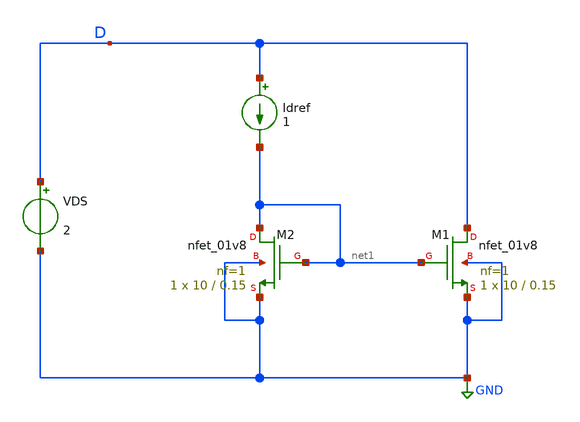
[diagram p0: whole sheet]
** sch_path: tb_ft_test.sch
**.subckt tb_ft_test
XM1 D net1 GND GND sky130_fd_pr__nfet_01v8 L=0.15 W=10 nf=1 ad='int((nf+1)/2) * W/nf * 0.29' as='int((nf+2)/2) * W/nf * 0.29'
+ pd='2*int((nf+1)/2) * (W/nf + 0.29)' ps='2*int((nf+2)/2) * (W/nf + 0.29)' nrd='0.29 / W' nrs='0.29 / W'
+ sa=0 sb=0 sd=0 mult=1 m=1
VDS D GND 2
Idref D net1 1
XM2 net1 net1 GND GND sky130_fd_pr__nfet_01v8 L=0.15 W=10 nf=1 ad='int((nf+1)/2) * W/nf * 0.29' as='int((nf+2)/2) * W/nf * 0.29'
+ pd='2*int((nf+1)/2) * (W/nf + 0.29)' ps='2*int((nf+2)/2) * (W/nf + 0.29)' nrd='0.29 / W' nrs='0.29 / W'
+ sa=0 sb=0 sd=0 mult=1 m=1
**** begin user architecture code



** Check the two ac lines below for being equal!
.options filetype=ascii
.save all

.op
.control
*dc Idref 0.1e-3 10e-3 0.1e-3

let n_idx = 101

let start_iref = 1e-6
let stop_iref = 10e-3
let delta_iref = (stop_iref - start_iref) / n_idx
let iref_act = start_iref

let gms = unitvec(n_idx)
let ids = unitvec(n_idx)

let cgss = unitvec(n_idx)
let cgds = unitvec(n_idx)

let idxs = 0
let idx = idxs

*loop
while iref_act le stop_iref
  alter idref iref_act
  run
  *print @m.xm2.msky130_fd_pr__nfet_01v8[gm]

  let gms[idx] = @m.xm2.msky130_fd_pr__nfet_01v8[gm]
  let ids[idx] = @m.xm2.msky130_fd_pr__nfet_01v8[id]

  let cgss[idx] = @m.xm2.msky130_fd_pr__nfet_01v8[cgs]
  let cgds[idx] = @m.xm2.msky130_fd_pr__nfet_01v8[cgd]

  let iref_act = iref_act + delta_iref
  let idxs = idx + 1
  let idx = idxs
end

let ft = gms/(2*3.1415*(cgss+cgds))

plot gms vs ids
plot xlog ft vs ids

.endc
.end



.include $::SKYWATER_MODELS/cells/nfet_01v8/sky130_fd_pr__nfet_01v8__tt.corner.spice
.include $::SKYWATER_MODELS/cells/nfet_01v8_lvt/sky130_fd_pr__nfet_01v8_lvt__tt.corner.spice
.include $::SKYWATER_MODELS/cells/pfet_01v8/sky130_fd_pr__pfet_01v8__tt.corner.spice
.include $::SKYWATER_MODELS/cells/nfet_03v3_nvt/sky130_fd_pr__nfet_03v3_nvt__tt.corner.spice
.include $::SKYWATER_MODELS/cells/nfet_05v0_nvt/sky130_fd_pr__nfet_05v0_nvt__tt.corner.spice
.include $::SKYWATER_MODELS/cells/esd_nfet_01v8/sky130_fd_pr__esd_nfet_01v8__tt.corner.spice
.include $::SKYWATER_MODELS/cells/pfet_01v8_lvt/sky130_fd_pr__pfet_01v8_lvt__tt.corner.spice
.include $::SKYWATER_MODELS/cells/pfet_01v8_hvt/sky130_fd_pr__pfet_01v8_hvt__tt.corner.spice
.include $::SKYWATER_MODELS/cells/esd_pfet_g5v0d10v5/sky130_fd_pr__esd_pfet_g5v0d10v5__tt.corner.spice
.include $::SKYWATER_MODELS/cells/pfet_g5v0d10v5/sky130_fd_pr__pfet_g5v0d10v5__tt.corner.spice
.include $::SKYWATER_MODELS/cells/pfet_g5v0d16v0/sky130_fd_pr__pfet_g5v0d16v0__tt.corner.spice
.include $::SKYWATER_MODELS/cells/nfet_g5v0d10v5/sky130_fd_pr__nfet_g5v0d10v5__tt.corner.spice
.include $::SKYWATER_MODELS/cells/nfet_g5v0d16v0/sky130_fd_pr__nfet_g5v0d16v0__tt_discrete.corner.spice
.include $::SKYWATER_MODELS/cells/esd_nfet_g5v0d10v5/sky130_fd_pr__esd_nfet_g5v0d10v5__tt.corner.spice
.include $::SKYWATER_MODELS/models/corners/tt/nonfet.spice
* Mismatch parameters
.include $::SKYWATER_MODELS/cells/nfet_01v8/sky130_fd_pr__nfet_01v8__mismatch.corner.spice
.include $::SKYWATER_MODELS/cells/pfet_01v8/sky130_fd_pr__pfet_01v8__mismatch.corner.spice
.include $::SKYWATER_MODELS/cells/nfet_01v8_lvt/sky130_fd_pr__nfet_01v8_lvt__mismatch.corner.spice
.include $::SKYWATER_MODELS/cells/pfet_01v8_lvt/sky130_fd_pr__pfet_01v8_lvt__mismatch.corner.spice
.include $::SKYWATER_MODELS/cells/pfet_01v8_hvt/sky130_fd_pr__pfet_01v8_hvt__mismatch.corner.spice
.include $::SKYWATER_MODELS/cells/nfet_g5v0d10v5/sky130_fd_pr__nfet_g5v0d10v5__mismatch.corner.spice
.include $::SKYWATER_MODELS/cells/pfet_g5v0d10v5/sky130_fd_pr__pfet_g5v0d10v5__mismatch.corner.spice
.include $::SKYWATER_MODELS/cells/nfet_05v0_nvt/sky130_fd_pr__nfet_05v0_nvt__mismatch.corner.spice
.include $::SKYWATER_MODELS/cells/nfet_03v3_nvt/sky130_fd_pr__nfet_03v3_nvt__mismatch.corner.spice
* Resistor$::SKYWATER_MODELS/Capacitor
.include $::SKYWATER_MODELS/models/r+c/res_typical__cap_typical.spice
.include $::SKYWATER_MODELS/models/r+c/res_typical__cap_typical__lin.spice
* Special cells
.include $::SKYWATER_MODELS/models/corners/tt/specialized_cells.spice
* All models
.include $::SKYWATER_MODELS/models/all.spice
* Corner
.include $::SKYWATER_MODELS/models/corners/tt/rf.spice

**** end user architecture code
**.ends
.GLOBAL GND
.end
